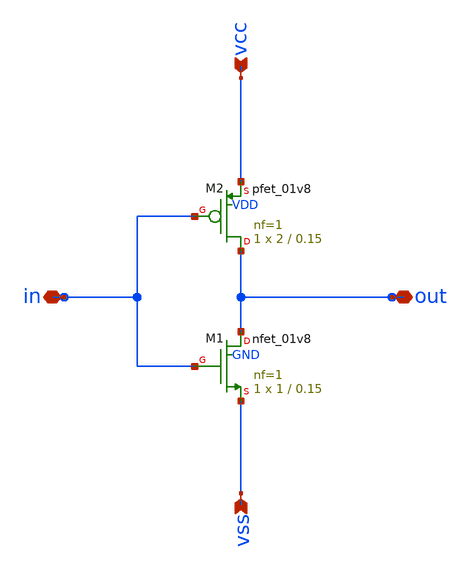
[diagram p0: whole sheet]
** sch_path: pll/ring_vco_lib/QRO_cell/xschem/core_cell.sch
**.subckt core_cell vcc vss in out
*.ipin vcc
*.ipin vss
*.iopin in
*.iopin out
XM1 out in vss GND sky130_fd_pr__nfet_01v8 L=0.15 W=1 nf=1 ad='int((nf+1)/2) * W/nf * 0.29' as='int((nf+2)/2) * W/nf * 0.29'
+ pd='2*int((nf+1)/2) * (W/nf + 0.29)' ps='2*int((nf+2)/2) * (W/nf + 0.29)' nrd='0.29 / W' nrs='0.29 / W'
+ sa=0 sb=0 sd=0 mult=1 m=1
XM2 out in vcc VDD sky130_fd_pr__pfet_01v8 L=0.15 W=2 nf=1 ad='int((nf+1)/2) * W/nf * 0.29' as='int((nf+2)/2) * W/nf * 0.29'
+ pd='2*int((nf+1)/2) * (W/nf + 0.29)' ps='2*int((nf+2)/2) * (W/nf + 0.29)' nrd='0.29 / W' nrs='0.29 / W'
+ sa=0 sb=0 sd=0 mult=1 m=1
**.ends
.end
